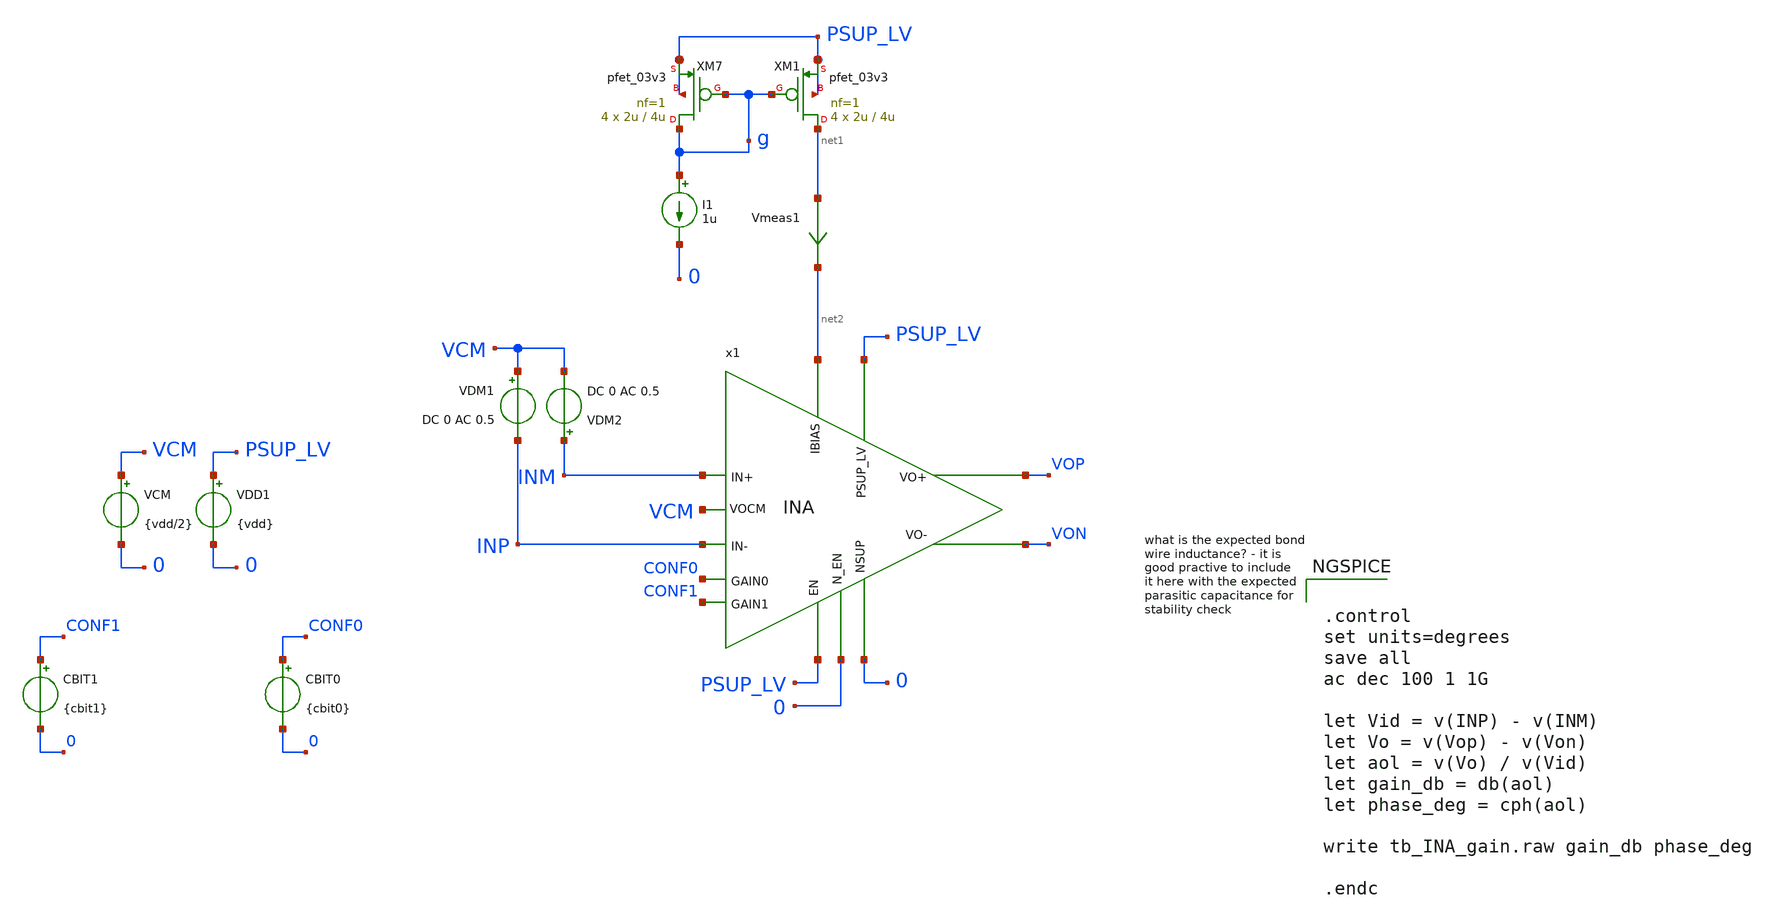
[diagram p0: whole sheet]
** sch_path: xschem/blocks/INA/tb_INA_gain.sch
**.subckt tb_INA_gain
VDD1 PSUP_LV 0 {vdd}
VCM VCM 0 {vdd/2}
VDM2 INM VCM DC 0 AC 0.5
VDM1 VCM INP DC 0 AC 0.5
x1 PSUP_LV 0 PSUP_LV 0 net2 CONF0 CONF1 INM VOP VCM INP VON INA
XM7 g g PSUP_LV PSUP_LV pfet_03v3 L=4u W=2u nf=1 ad='int((nf+1)/2) * W/nf * 0.18u' as='int((nf+2)/2) * W/nf * 0.18u'
+ pd='2*int((nf+1)/2) * (W/nf + 0.18u)' ps='2*int((nf+2)/2) * (W/nf + 0.18u)' nrd='0.18u / W' nrs='0.18u / W'
+ sa=0 sb=0 sd=0 m=4
XM1 net1 g PSUP_LV PSUP_LV pfet_03v3 L=4u W=2u nf=1 ad='int((nf+1)/2) * W/nf * 0.18u' as='int((nf+2)/2) * W/nf * 0.18u'
+ pd='2*int((nf+1)/2) * (W/nf + 0.18u)' ps='2*int((nf+2)/2) * (W/nf + 0.18u)' nrd='0.18u / W' nrs='0.18u / W'
+ sa=0 sb=0 sd=0 m=4
I1 g 0 1u
Vmeas1 net1 net2 0
.save i(vmeas1)
CBIT1 CONF1 0 {cbit1}
CBIT0 CONF0 0 {cbit0}
**** begin user architecture code

.include $::180MCU_MODELS/design.ngspice

.lib $::180MCU_MODELS/sm141064.ngspice typical
.lib $::180MCU_MODELS/sm141064.ngspice res_typical
.lib $::180MCU_MODELS/sm141064.ngspice bjt_typical
.lib $::180MCU_MODELS/sm141064.ngspice mimcap_typical
.lib $::180MCU_MODELS/sm141064.ngspice cap_mim

.temp 25

.param vdd=3.3

.param cbit0=0
.param cbit1=0
.param cbit2=0

* Deterministic PVT: disable random global/mismatch variation.
.param sw_stat_global=0
.param sw_stat_mismatch=0



.control
set units=degrees
save all
ac dec 100 1 1G

let Vid = v(INP) - v(INM)
let Vo = v(Vop) - v(Von)
let aol = v(Vo) / v(Vid)
let gain_db = db(aol)
let phase_deg = cph(aol)

write tb_INA_gain.raw gain_db phase_deg

.endc


**** end user architecture code
**.ends
.end
